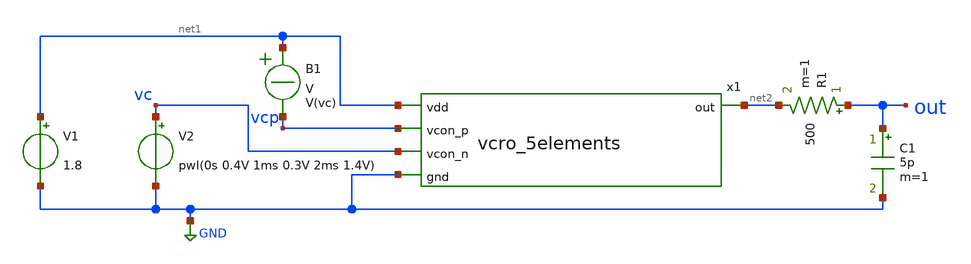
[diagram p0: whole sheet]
** sch_path: xschem/vcro_5st_tb.sch
**.subckt vcro_5st_tb
V1 net1 GND 1.8
V2 vc GND pwl(0s 0.4V 1ms 0.3V 2ms 1.4V)
R1 out net2 500 m=1
B1 net1 vcp V = V(vc)
x1 net2 net1 vcp vc GND vcro_5elements
C1 out GND 5p m=1
**** begin user architecture code
 .lib $::SKYWATER_MODELS/sky130.lib.spice tt

.param mc_mm_switch=0
.param mc_pr_switch=1



.option wnflag=0
.option savecurrents
.control
save all
tran 10n 2m 1m
plot vc vcp out
plot i(V1)
write vcro5.raw
op
.endc


**** end user architecture code
**.ends
.GLOBAL GND
.end
